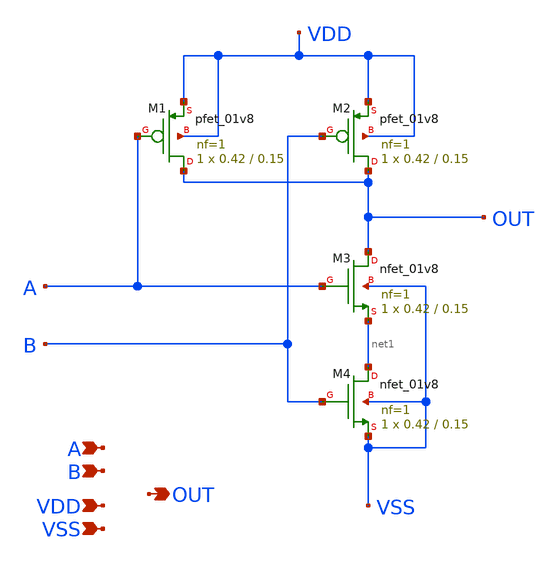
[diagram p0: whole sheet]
** sch_path: test_RO/nand/nand.sch
**.subckt nand A OUT B VDD VSS
*.ipin A
*.opin OUT
*.ipin B
*.ipin VDD
*.ipin VSS
XM1 OUT A VDD VDD sky130_fd_pr__pfet_01v8 L=0.15 W=0.42 nf=1 ad='int((nf+1)/2) * W/nf * 0.29' as='int((nf+2)/2) * W/nf * 0.29'
+ pd='2*int((nf+1)/2) * (W/nf + 0.29)' ps='2*int((nf+2)/2) * (W/nf + 0.29)' nrd='0.29 / W' nrs='0.29 / W'
+ sa=0 sb=0 sd=0 mult=1 m=1
XM2 OUT B VDD VDD sky130_fd_pr__pfet_01v8 L=0.15 W=0.42 nf=1 ad='int((nf+1)/2) * W/nf * 0.29' as='int((nf+2)/2) * W/nf * 0.29'
+ pd='2*int((nf+1)/2) * (W/nf + 0.29)' ps='2*int((nf+2)/2) * (W/nf + 0.29)' nrd='0.29 / W' nrs='0.29 / W'
+ sa=0 sb=0 sd=0 mult=1 m=1
XM3 OUT A net1 VSS sky130_fd_pr__nfet_01v8 L=0.15 W=0.42 nf=1 ad='int((nf+1)/2) * W/nf * 0.29' as='int((nf+2)/2) * W/nf * 0.29'
+ pd='2*int((nf+1)/2) * (W/nf + 0.29)' ps='2*int((nf+2)/2) * (W/nf + 0.29)' nrd='0.29 / W' nrs='0.29 / W'
+ sa=0 sb=0 sd=0 mult=1 m=1
XM4 net1 B VSS VSS sky130_fd_pr__nfet_01v8 L=0.15 W=0.42 nf=1 ad='int((nf+1)/2) * W/nf * 0.29' as='int((nf+2)/2) * W/nf * 0.29'
+ pd='2*int((nf+1)/2) * (W/nf + 0.29)' ps='2*int((nf+2)/2) * (W/nf + 0.29)' nrd='0.29 / W' nrs='0.29 / W'
+ sa=0 sb=0 sd=0 mult=1 m=1
**.ends
.end
